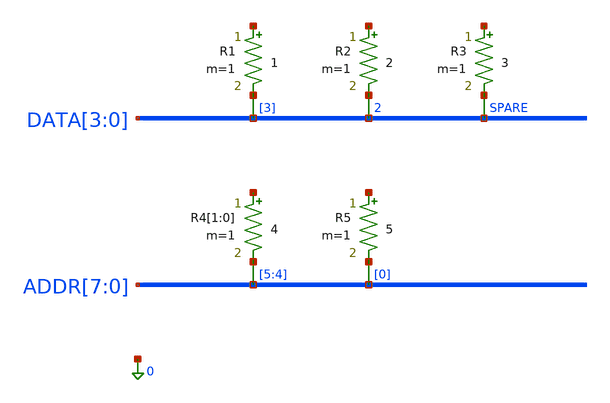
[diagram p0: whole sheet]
** sch_path: tests/golden/SCHEM/cases/SCHEM-NL-19/input/nl19.sch
**.subckt nl19
R1 net1 DATA[3] 1 m=1
R2 net2 DATA2 2 m=1
R3 net3 SPARE 3 m=1
R4[1] net4[1] ADDR[5] 4 m=1
R4[0] net4[0] ADDR[4] 4 m=1
R5 net5 ADDR[0] 5 m=1
**.ends
.end
